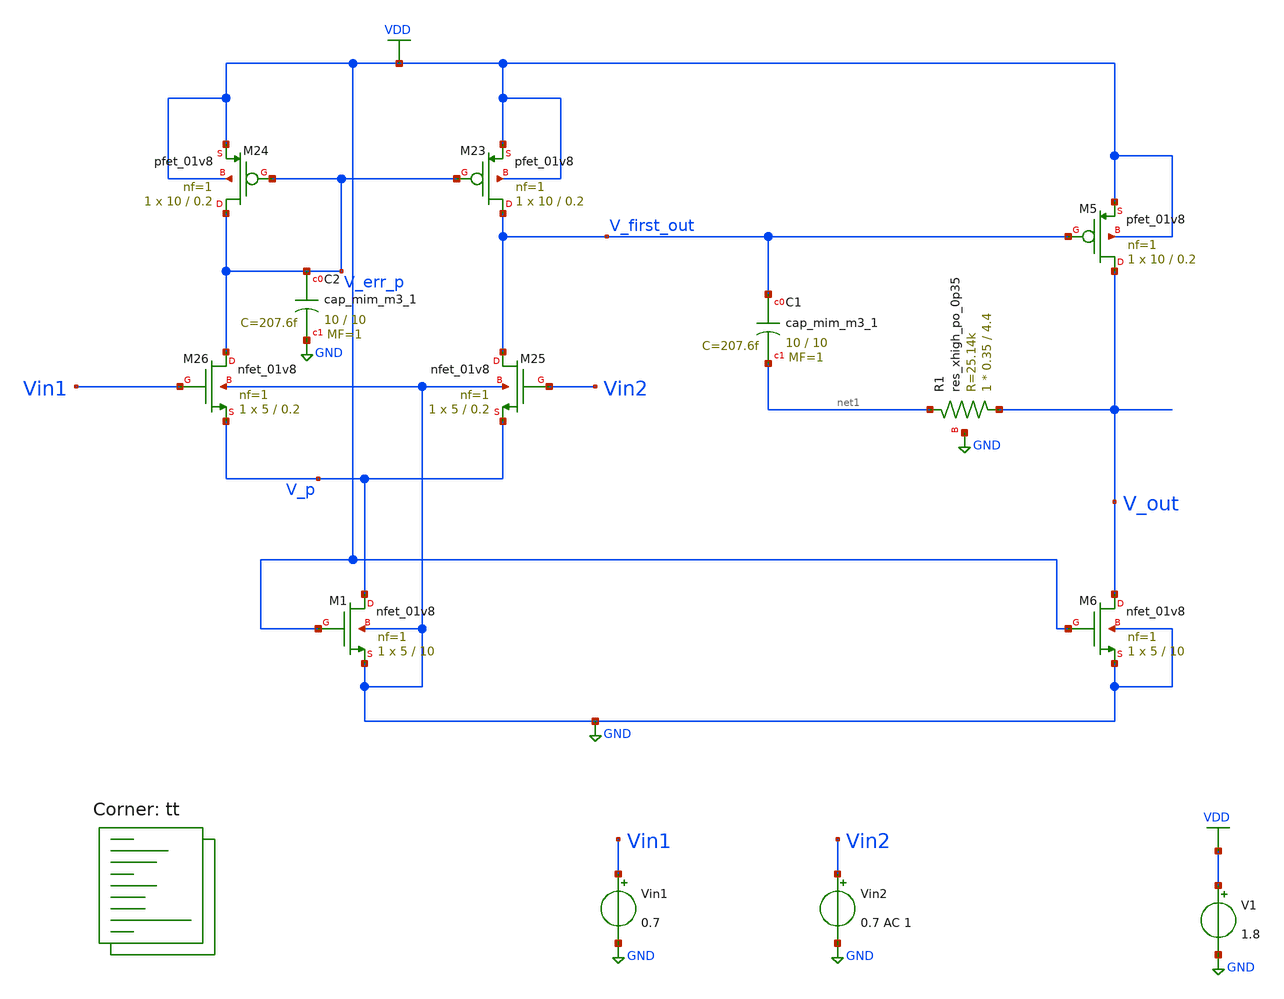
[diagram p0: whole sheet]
** sch_path: projects/bandgapref/xschem_ngspice/new_files/tb_opamp_bandgap_2.sch
**.subckt tb_opamp_bandgap_2
V1 VDD GND 1.8
Vin1 Vin1 GND 0.7
Vin2 Vin2 GND 0.7 AC 1
XM23 V_first_out V_err_p VDD VDD sky130_fd_pr__pfet_01v8 L=0.2 W=10 nf=1 ad='int((nf+1)/2) * W/nf * 0.29'
+ as='int((nf+2)/2) * W/nf * 0.29' pd='2*int((nf+1)/2) * (W/nf + 0.29)' ps='2*int((nf+2)/2) * (W/nf + 0.29)'
+ nrd='0.29 / W' nrs='0.29 / W' sa=0 sb=0 sd=0 mult=1 m=1
XM24 V_err_p V_err_p VDD VDD sky130_fd_pr__pfet_01v8 L=0.2 W=10 nf=1 ad='int((nf+1)/2) * W/nf * 0.29'
+ as='int((nf+2)/2) * W/nf * 0.29' pd='2*int((nf+1)/2) * (W/nf + 0.29)' ps='2*int((nf+2)/2) * (W/nf + 0.29)'
+ nrd='0.29 / W' nrs='0.29 / W' sa=0 sb=0 sd=0 mult=1 m=1
XM25 V_first_out Vin2 V_p GND sky130_fd_pr__nfet_01v8 L=0.2 W=5 nf=1 ad='int((nf+1)/2) * W/nf * 0.29'
+ as='int((nf+2)/2) * W/nf * 0.29' pd='2*int((nf+1)/2) * (W/nf + 0.29)' ps='2*int((nf+2)/2) * (W/nf + 0.29)'
+ nrd='0.29 / W' nrs='0.29 / W' sa=0 sb=0 sd=0 mult=1 m=1
XM26 V_err_p Vin1 V_p GND sky130_fd_pr__nfet_01v8 L=0.2 W=5 nf=1 ad='int((nf+1)/2) * W/nf * 0.29' as='int((nf+2)/2) * W/nf * 0.29'
+ pd='2*int((nf+1)/2) * (W/nf + 0.29)' ps='2*int((nf+2)/2) * (W/nf + 0.29)' nrd='0.29 / W' nrs='0.29 / W'
+ sa=0 sb=0 sd=0 mult=1 m=1
XM1 V_p VDD GND GND sky130_fd_pr__nfet_01v8 L=10 W=5 nf=1 ad='int((nf+1)/2) * W/nf * 0.29' as='int((nf+2)/2) * W/nf * 0.29'
+ pd='2*int((nf+1)/2) * (W/nf + 0.29)' ps='2*int((nf+2)/2) * (W/nf + 0.29)' nrd='0.29 / W' nrs='0.29 / W'
+ sa=0 sb=0 sd=0 mult=1 m=1
XM5 V_out V_first_out VDD VDD sky130_fd_pr__pfet_01v8 L=0.2 W=10 nf=1 ad='int((nf+1)/2) * W/nf * 0.29'
+ as='int((nf+2)/2) * W/nf * 0.29' pd='2*int((nf+1)/2) * (W/nf + 0.29)' ps='2*int((nf+2)/2) * (W/nf + 0.29)'
+ nrd='0.29 / W' nrs='0.29 / W' sa=0 sb=0 sd=0 mult=1 m=1
XM6 V_out VDD GND GND sky130_fd_pr__nfet_01v8 L=10 W=5 nf=1 ad='int((nf+1)/2) * W/nf * 0.29' as='int((nf+2)/2) * W/nf * 0.29'
+ pd='2*int((nf+1)/2) * (W/nf + 0.29)' ps='2*int((nf+2)/2) * (W/nf + 0.29)' nrd='0.29 / W' nrs='0.29 / W'
+ sa=0 sb=0 sd=0 mult=1 m=1
XC1 V_first_out net1 sky130_fd_pr__cap_mim_m3_1 W=10 L=10 MF=1 m=1
XR1 V_out net1 GND sky130_fd_pr__res_xhigh_po_0p35 L=4.4 mult=1 m=1
XC2 V_err_p GND sky130_fd_pr__cap_mim_m3_1 W=10 L=10 MF=1 m=1
**** begin user architecture code



.option wnflag=1
.option savecurrents

.save @m.xm1.msky130_fd_pr__nfet_01v8[gm] @m.xm2.msky130_fd_pr__nfet_01v8[gm] @m.xm3.msky130_fd_pr__nfet_01v8[gm] @m.xm4.msky130_fd_pr__pfet_01v8[gm] @m.xm5.msky130_fd_pr__pfet_01v8[gm] @m.xm6.msky130_fd_pr__nfet_01v8[gm] @m.xm7.msky130_fd_pr__pfet_01v8[gm]

.control

  save all
   * tran 1u 3m
   ac dec 20 1 1T

  write tb_opamp_bandgap_2.raw
  set appendwrite

.endc



.lib $::SKYWATER_MODELS/sky130.lib.spice tt
**** end user architecture code
**.ends
.GLOBAL GND
.GLOBAL VDD
.end
